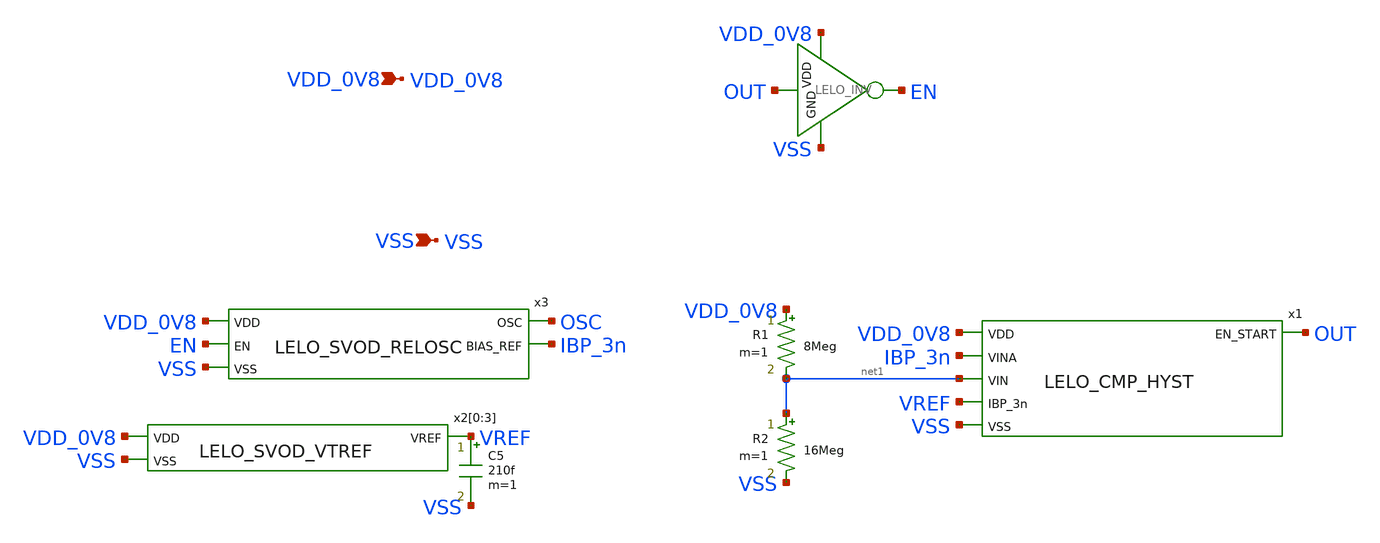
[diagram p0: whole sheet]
** sch_path: design/LELO_SVOD_SKY130A/LELO_STARTUP_DETECTOR_TEST.sch
**.subckt LELO_STARTUP_DETECTOR_TEST VSS VDD_0V8
*.ipin VSS
*.ipin VDD_0V8
x1 VDD_0V8 OUT IBP_3n net1 VREF VSS LELO_CMP_HYST
x2[0] VDD_0V8 VSS VREF LELO_SVOD_VTREF
x2[1] VDD_0V8 VSS VREF LELO_SVOD_VTREF
x2[2] VDD_0V8 VSS VREF LELO_SVOD_VTREF
x2[3] VDD_0V8 VSS VREF LELO_SVOD_VTREF
x3 VDD_0V8 OSC IBP_3n EN VSS LELO_SVOD_RELOSC
C5 VREF VSS 210f m=1
R1 VDD_0V8 net1 8Meg m=1
R2 net1 VSS 16Meg m=1
x2 VDD_0V8 OUT EN VSS LELO_INV
**.ends
.end
